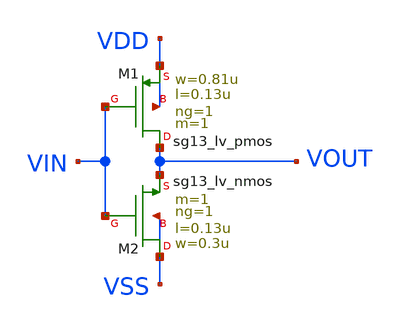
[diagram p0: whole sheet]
** sch_path: Taller3/Resuelto/inv.sch
**.subckt inv
XM2 VSS VIN VOUT VSS sg13_lv_nmos w=0.3u l=0.13u ng=1 m=1 mm_ok=1
XM1 VOUT VIN VDD VDD sg13_lv_pmos w=0.81u l=0.13u ng=1 m=1 mm_ok=1
**.ends
.end
